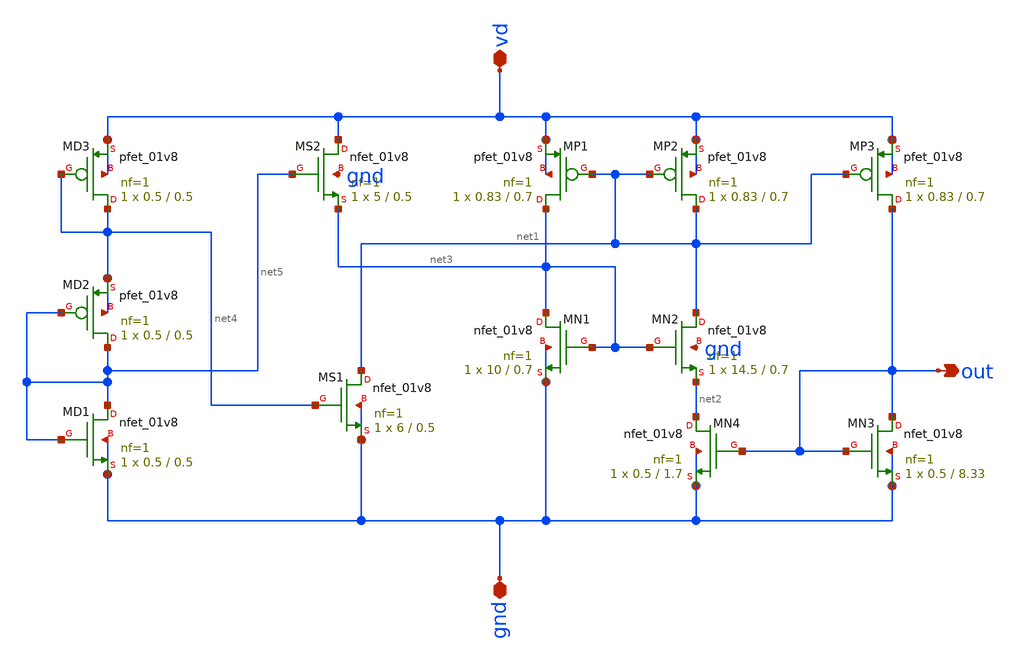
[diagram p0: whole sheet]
** sch_path: bandgap-ref/xschem/bandgap-ref.sch
**.subckt bandgap-ref vd gnd out
*.iopin vd
*.iopin gnd
*.opin out
XMN1 net3 net3 gnd gnd sky130_fd_pr__nfet_01v8 L=0.7 W=10 nf=1 ad='int((nf+1)/2) * W/nf * 0.29' as='int((nf+2)/2) * W/nf * 0.29'
+ pd='2*int((nf+1)/2) * (W/nf + 0.29)' ps='2*int((nf+2)/2) * (W/nf + 0.29)' nrd='0.29 / W' nrs='0.29 / W'
+ sa=0 sb=0 sd=0 mult=1 m=1
XMP1 net3 net1 vd vd sky130_fd_pr__pfet_01v8 L=0.7 W=0.83 nf=1 ad='int((nf+1)/2) * W/nf * 0.29' as='int((nf+2)/2) * W/nf * 0.29'
+ pd='2*int((nf+1)/2) * (W/nf + 0.29)' ps='2*int((nf+2)/2) * (W/nf + 0.29)' nrd='0.29 / W' nrs='0.29 / W'
+ sa=0 sb=0 sd=0 mult=1 m=1
XMP2 net1 net1 vd vd sky130_fd_pr__pfet_01v8 L=0.7 W=0.83 nf=1 ad='int((nf+1)/2) * W/nf * 0.29' as='int((nf+2)/2) * W/nf * 0.29'
+ pd='2*int((nf+1)/2) * (W/nf + 0.29)' ps='2*int((nf+2)/2) * (W/nf + 0.29)' nrd='0.29 / W' nrs='0.29 / W'
+ sa=0 sb=0 sd=0 mult=1 m=1
XMP3 out net1 vd vd sky130_fd_pr__pfet_01v8 L=0.7 W=0.83 nf=1 ad='int((nf+1)/2) * W/nf * 0.29' as='int((nf+2)/2) * W/nf * 0.29'
+ pd='2*int((nf+1)/2) * (W/nf + 0.29)' ps='2*int((nf+2)/2) * (W/nf + 0.29)' nrd='0.29 / W' nrs='0.29 / W'
+ sa=0 sb=0 sd=0 mult=1 m=1
XMN2 net1 net3 net2 gnd sky130_fd_pr__nfet_01v8 L=0.7 W=14.5 nf=1 ad='int((nf+1)/2) * W/nf * 0.29' as='int((nf+2)/2) * W/nf * 0.29'
+ pd='2*int((nf+1)/2) * (W/nf + 0.29)' ps='2*int((nf+2)/2) * (W/nf + 0.29)' nrd='0.29 / W' nrs='0.29 / W'
+ sa=0 sb=0 sd=0 mult=1 m=1
XMN3 out out gnd gnd sky130_fd_pr__nfet_01v8 L=8.33 W=0.5 nf=1 ad='int((nf+1)/2) * W/nf * 0.29' as='int((nf+2)/2) * W/nf * 0.29'
+ pd='2*int((nf+1)/2) * (W/nf + 0.29)' ps='2*int((nf+2)/2) * (W/nf + 0.29)' nrd='0.29 / W' nrs='0.29 / W'
+ sa=0 sb=0 sd=0 mult=1 m=1
XMN4 net2 out gnd gnd sky130_fd_pr__nfet_01v8 L=1.7 W=0.5 nf=1 ad='int((nf+1)/2) * W/nf * 0.29' as='int((nf+2)/2) * W/nf * 0.29'
+ pd='2*int((nf+1)/2) * (W/nf + 0.29)' ps='2*int((nf+2)/2) * (W/nf + 0.29)' nrd='0.29 / W' nrs='0.29 / W'
+ sa=0 sb=0 sd=0 mult=1 m=1
XMS2 vd net5 net3 gnd sky130_fd_pr__nfet_01v8 L=0.5 W=5 nf=1 ad='int((nf+1)/2) * W/nf * 0.29' as='int((nf+2)/2) * W/nf * 0.29'
+ pd='2*int((nf+1)/2) * (W/nf + 0.29)' ps='2*int((nf+2)/2) * (W/nf + 0.29)' nrd='0.29 / W' nrs='0.29 / W'
+ sa=0 sb=0 sd=0 mult=1 m=1
XMS1 net1 net4 gnd gnd sky130_fd_pr__nfet_01v8 L=0.5 W=6 nf=1 ad='int((nf+1)/2) * W/nf * 0.29' as='int((nf+2)/2) * W/nf * 0.29'
+ pd='2*int((nf+1)/2) * (W/nf + 0.29)' ps='2*int((nf+2)/2) * (W/nf + 0.29)' nrd='0.29 / W' nrs='0.29 / W'
+ sa=0 sb=0 sd=0 mult=1 m=1
XMD3 net4 net4 vd vd sky130_fd_pr__pfet_01v8 L=0.5 W=0.5 nf=1 ad='int((nf+1)/2) * W/nf * 0.29' as='int((nf+2)/2) * W/nf * 0.29'
+ pd='2*int((nf+1)/2) * (W/nf + 0.29)' ps='2*int((nf+2)/2) * (W/nf + 0.29)' nrd='0.29 / W' nrs='0.29 / W'
+ sa=0 sb=0 sd=0 mult=1 m=1
XMD2 net5 net5 net4 net4 sky130_fd_pr__pfet_01v8 L=0.5 W=0.5 nf=1 ad='int((nf+1)/2) * W/nf * 0.29' as='int((nf+2)/2) * W/nf * 0.29'
+ pd='2*int((nf+1)/2) * (W/nf + 0.29)' ps='2*int((nf+2)/2) * (W/nf + 0.29)' nrd='0.29 / W' nrs='0.29 / W'
+ sa=0 sb=0 sd=0 mult=1 m=1
XMD1 net5 net5 gnd gnd sky130_fd_pr__nfet_01v8 L=0.5 W=0.5 nf=1 ad='int((nf+1)/2) * W/nf * 0.29' as='int((nf+2)/2) * W/nf * 0.29'
+ pd='2*int((nf+1)/2) * (W/nf + 0.29)' ps='2*int((nf+2)/2) * (W/nf + 0.29)' nrd='0.29 / W' nrs='0.29 / W'
+ sa=0 sb=0 sd=0 mult=1 m=1
**.ends
.end
